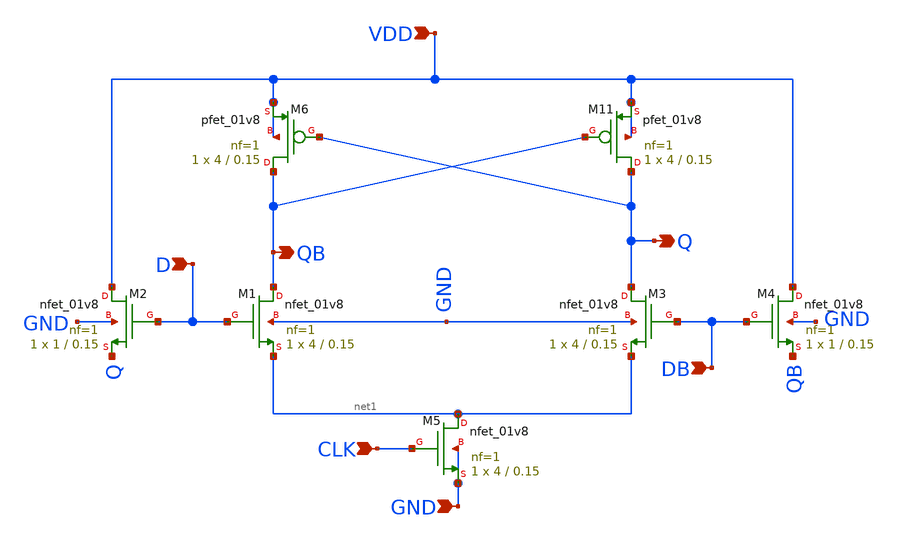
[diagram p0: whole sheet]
** sch_path: pll/dividers_lib/divider_design_trials/Testbench for testing latches/dynamic_latch.sch
**.subckt dynamic_latch VDD D Q GND CLK DB QB
*.ipin VDD
*.ipin D
*.opin Q
*.ipin GND
*.ipin CLK
*.ipin DB
*.opin QB
XM11 Q QB VDD VDD sky130_fd_pr__pfet_01v8 L=0.15 W=4 nf=1 ad='int((nf+1)/2) * W/nf * 0.29' as='int((nf+2)/2) * W/nf * 0.29'
+ pd='2*int((nf+1)/2) * (W/nf + 0.29)' ps='2*int((nf+2)/2) * (W/nf + 0.29)' nrd='0.29 / W' nrs='0.29 / W'
+ sa=0 sb=0 sd=0 mult=1 m=1
XM2 VDD D Q GND sky130_fd_pr__nfet_01v8 L=0.15 W=1 nf=1 ad='int((1 + 1)/2) * 1 / 1 * 0.29' as='int((1 + 2)/2) * 1 / 1 * 0.29'
+ pd='2*int((1 + 1)/2) * (1 / 1 + 0.29)' ps='2*int((1 + 2)/2) * (1 / 1 + 0.29)' nrd='0.29 / 1 ' nrs='0.29 / 1 '
+ sa=0 sb=0 sd=0 mult=1 m=1
XM4 VDD DB QB GND sky130_fd_pr__nfet_01v8 L=0.15 W=1 nf=1 ad='int((1 + 1)/2) * 1 / 1 * 0.29' as='int((1 + 2)/2) * 1 / 1 * 0.29'
+ pd='2*int((1 + 1)/2) * (1 / 1 + 0.29)' ps='2*int((1 + 2)/2) * (1 / 1 + 0.29)' nrd='0.29 / 1 ' nrs='0.29 / 1 '
+ sa=0 sb=0 sd=0 mult=1 m=1
XM6 QB Q VDD VDD sky130_fd_pr__pfet_01v8 L=0.15 W=4 nf=1 ad='int((nf+1)/2) * W/nf * 0.29' as='int((nf+2)/2) * W/nf * 0.29'
+ pd='2*int((nf+1)/2) * (W/nf + 0.29)' ps='2*int((nf+2)/2) * (W/nf + 0.29)' nrd='0.29 / W' nrs='0.29 / W'
+ sa=0 sb=0 sd=0 mult=1 m=1
XM1 QB D net1 GND sky130_fd_pr__nfet_01v8 L=0.15 W=4 nf=1 ad='int((1 + 1)/2) * 4 / 1 * 0.29' as='int((1 + 2)/2) * 4 / 1 * 0.29'
+ pd='2*int((1 + 1)/2) * (4 / 1 + 0.29)' ps='2*int((1 + 2)/2) * (4 / 1 + 0.29)' nrd='0.29 / 4 ' nrs='0.29 / 4 '
+ sa=0 sb=0 sd=0 mult=1 m=1
XM3 Q DB net1 GND sky130_fd_pr__nfet_01v8 L=0.15 W=4 nf=1 ad='int((1 + 1)/2) * 4 / 1 * 0.29' as='int((1 + 2)/2) * 4 / 1 * 0.29'
+ pd='2*int((1 + 1)/2) * (4 / 1 + 0.29)' ps='2*int((1 + 2)/2) * (4 / 1 + 0.29)' nrd='0.29 / 4 ' nrs='0.29 / 4 '
+ sa=0 sb=0 sd=0 mult=1 m=1
XM5 net1 CLK GND GND sky130_fd_pr__nfet_01v8 L=0.15 W=4 nf=1 ad='int((1 + 1)/2) * 4 / 1 * 0.29' as='int((1 + 2)/2) * 4 / 1 * 0.29'
+ pd='2*int((1 + 1)/2) * (4 / 1 + 0.29)' ps='2*int((1 + 2)/2) * (4 / 1 + 0.29)' nrd='0.29 / 4 ' nrs='0.29 / 4 '
+ sa=0 sb=0 sd=0 mult=1 m=1
**.ends
.end
